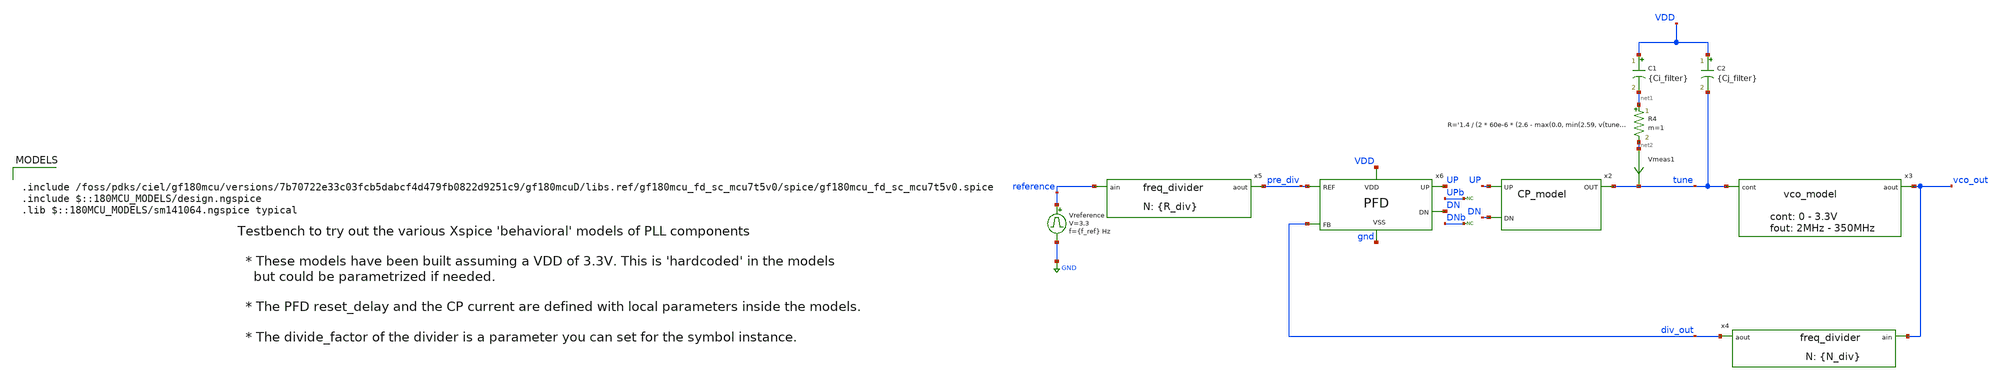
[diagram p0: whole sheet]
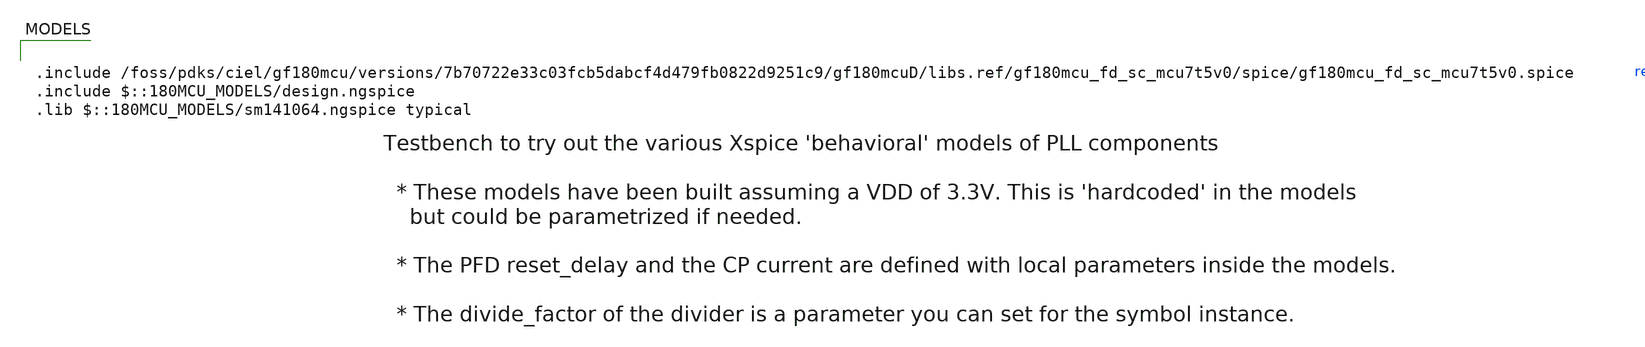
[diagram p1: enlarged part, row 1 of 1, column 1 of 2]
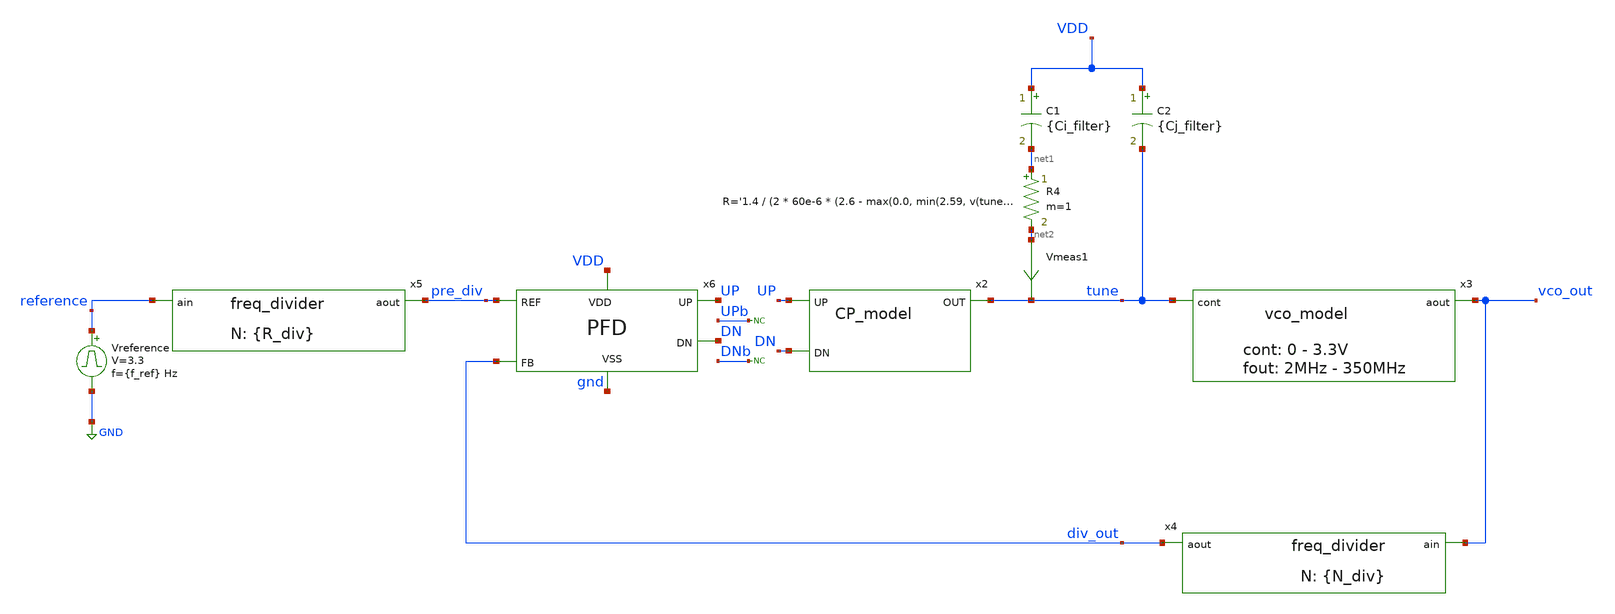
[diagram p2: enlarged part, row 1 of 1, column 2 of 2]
** sch_path: designs/libs/tb_pll/tb_PLL_PFD_model.sch
**.subckt tb_PLL_PFD_model
Vreference reference GND pulse 0 3.3 '0.495/ {f_ref} ' '0.01/{f_ref} ' '0.01/{f_ref} ' '0.49/{f_ref} '
+ '1/{f_ref} '
C1 VDD net1 {Ci_filter} m=1
R4 net1 net2 R='1.4 / (2 * 60e-6 * (2.6 - max(0.0, min(2.59, v(tune)))))' m=1
* noconn DNb
* noconn UPb
C2 VDD tune {Cj_filter} m=1
x2 tune UP DN CP_model
x3 vco_out tune vco_model
x4 div_out vco_out freq_divider divide_factor={N_div}
Vmeas1 net2 tune 0
.save i(vmeas1)
x5 pre_div reference freq_divider divide_factor={R_div}
x6 pre_div UP DN div_out VDD gnd pfd
**** begin user architecture code


.control
set wr_singlescale
set wr_vecnames
save all
TRAN 1n 500u 0 100p
remzerovec
*linearize v(vco_out)
write tb_PLL_PFD_model.raw
wrdata /foss/designs/synchronos-chipathon-2026/designs/libs/scripts/sim_data/tb_PLL_PFD_model.txt
+ tran.all
*fft v(vco_out)
*plot mag(v(vco_out)) xlimit 10k 2G xlog ylog
.endc




.options method=gear
.options reltol=1e-5
VDD VDD 0 3.3
* control is for tests when opening the loop
* see the Vcontrol voltage source
.ic v(tune)=2.6
* reference frequency
.param f_ref = 10MEG
* divider
.param R_div=10
.param N_div=70
* loop filter parameters
.param Ci_filter = 10p
.param Cj_filter = 1p



.include /foss/pdks/ciel/gf180mcu/versions/7b70722e33c03fcb5dabcf4d479fb0822d9251c9/gf180mcuD/libs.ref/gf180mcu_fd_sc_mcu7t5v0/spice/gf180mcu_fd_sc_mcu7t5v0.spice
.include $::180MCU_MODELS/design.ngspice
.lib $::180MCU_MODELS/sm141064.ngspice typical

**** end user architecture code
**.ends
.GLOBAL GND
.end
